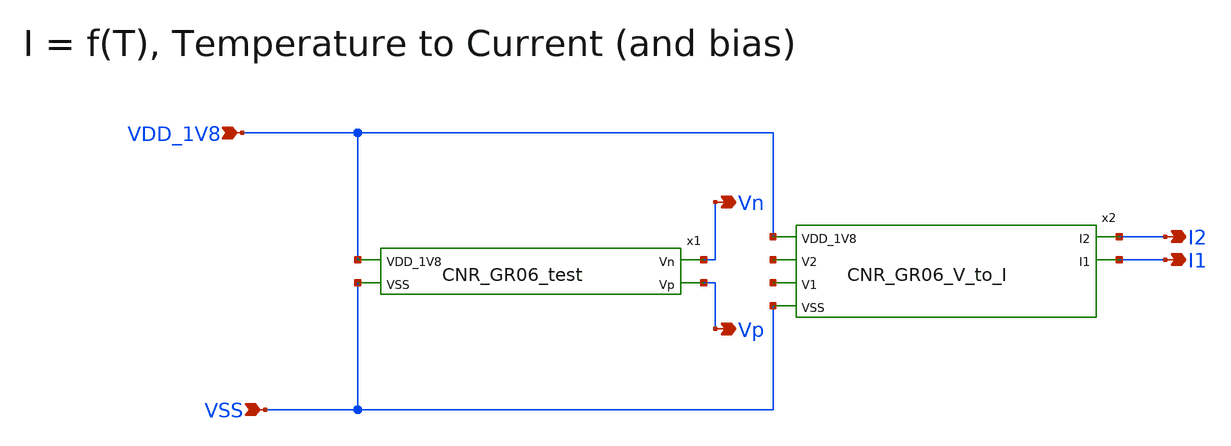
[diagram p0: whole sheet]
** sch_path: design/CNR_GR06_SKY130NM/CNR_GR06.sch
**.subckt CNR_GR06 VDD_1V8 VSS I2 I1 Vn Vp
*.ipin VDD_1V8
*.ipin VSS
*.opin I2
*.opin I1
*.opin Vn
*.opin Vp
x1 VDD_1V8 Vn Vp VSS CNR_GR06_test
x2 VDD_1V8 I2 I1 net1 net2 VSS CNR_GR06_V_to_I
**.ends

* expanding   symbol:  CNR_GR06_SKY130NM/CNR_GR06_test.sym # of pins=4
** sym_path: design/CNR_GR06_SKY130NM/CNR_GR06_test.sym
** sch_path: design/CNR_GR06_SKY130NM/CNR_GR06_test.sch
.subckt CNR_GR06_test VDD_1V8 Vn Vp VSS
*.ipin VSS
*.opin Vn
*.opin Vp
*.ipin VDD_1V8
XM1 net14 net1 VDD_1V8 VDD_1V8 sky130_fd_pr__pfet_01v8 L=1 W=20 nf=1 ad='int((nf+1)/2) * W/nf * 0.29'
+ as='int((nf+2)/2) * W/nf * 0.29' pd='2*int((nf+1)/2) * (W/nf + 0.29)' ps='2*int((nf+2)/2) * (W/nf + 0.29)'
+ nrd='0.29 / W' nrs='0.29 / W' sa=0 sb=0 sd=0 mult=1 m=1
XM3 net1 net1 VDD_1V8 VDD_1V8 sky130_fd_pr__pfet_01v8 L=1 W=20 nf=1 ad='int((nf+1)/2) * W/nf * 0.29'
+ as='int((nf+2)/2) * W/nf * 0.29' pd='2*int((nf+1)/2) * (W/nf + 0.29)' ps='2*int((nf+2)/2) * (W/nf + 0.29)'
+ nrd='0.29 / W' nrs='0.29 / W' sa=0 sb=0 sd=0 mult=1 m=1
XM4 net1 net1 VDD_1V8 VDD_1V8 sky130_fd_pr__pfet_01v8 L=1 W=20 nf=1 ad='int((nf+1)/2) * W/nf * 0.29'
+ as='int((nf+2)/2) * W/nf * 0.29' pd='2*int((nf+1)/2) * (W/nf + 0.29)' ps='2*int((nf+2)/2) * (W/nf + 0.29)'
+ nrd='0.29 / W' nrs='0.29 / W' sa=0 sb=0 sd=0 mult=1 m=1
XM5 net15 net1 VDD_1V8 VDD_1V8 sky130_fd_pr__pfet_01v8 L=1 W=20 nf=1 ad='int((nf+1)/2) * W/nf * 0.29'
+ as='int((nf+2)/2) * W/nf * 0.29' pd='2*int((nf+1)/2) * (W/nf + 0.29)' ps='2*int((nf+2)/2) * (W/nf + 0.29)'
+ nrd='0.29 / W' nrs='0.29 / W' sa=0 sb=0 sd=0 mult=1 m=1
XM6 net3 net2 net14 VDD_1V8 sky130_fd_pr__pfet_01v8 L=1 W=20 nf=1 ad='int((nf+1)/2) * W/nf * 0.29' as='int((nf+2)/2) * W/nf * 0.29'
+ pd='2*int((nf+1)/2) * (W/nf + 0.29)' ps='2*int((nf+2)/2) * (W/nf + 0.29)' nrd='0.29 / W' nrs='0.29 / W'
+ sa=0 sb=0 sd=0 mult=1 m=1
XM8 net2 net2 net1 VDD_1V8 sky130_fd_pr__pfet_01v8 L=1 W=20 nf=1 ad='int((nf+1)/2) * W/nf * 0.29' as='int((nf+2)/2) * W/nf * 0.29'
+ pd='2*int((nf+1)/2) * (W/nf + 0.29)' ps='2*int((nf+2)/2) * (W/nf + 0.29)' nrd='0.29 / W' nrs='0.29 / W'
+ sa=0 sb=0 sd=0 mult=1 m=1
XM9 net2 net2 net1 VDD_1V8 sky130_fd_pr__pfet_01v8 L=1 W=20 nf=1 ad='int((nf+1)/2) * W/nf * 0.29' as='int((nf+2)/2) * W/nf * 0.29'
+ pd='2*int((nf+1)/2) * (W/nf + 0.29)' ps='2*int((nf+2)/2) * (W/nf + 0.29)' nrd='0.29 / W' nrs='0.29 / W'
+ sa=0 sb=0 sd=0 mult=1 m=1
XM10 net4 net2 net15 VDD_1V8 sky130_fd_pr__pfet_01v8 L=1 W=20 nf=1 ad='int((nf+1)/2) * W/nf * 0.29' as='int((nf+2)/2) * W/nf * 0.29'
+ pd='2*int((nf+1)/2) * (W/nf + 0.29)' ps='2*int((nf+2)/2) * (W/nf + 0.29)' nrd='0.29 / W' nrs='0.29 / W'
+ sa=0 sb=0 sd=0 mult=1 m=1
XM11 net3 net3 VSS VSS sky130_fd_pr__nfet_01v8 L=1 W=10 nf=1 ad='int((nf+1)/2) * W/nf * 0.29' as='int((nf+2)/2) * W/nf * 0.29'
+ pd='2*int((nf+1)/2) * (W/nf + 0.29)' ps='2*int((nf+2)/2) * (W/nf + 0.29)' nrd='0.29 / W' nrs='0.29 / W'
+ sa=0 sb=0 sd=0 mult=1 m=1
XM12 net2 net3 net5 VSS sky130_fd_pr__nfet_01v8 L=1 W=10 nf=1 ad='int((nf+1)/2) * W/nf * 0.29' as='int((nf+2)/2) * W/nf * 0.29'
+ pd='2*int((nf+1)/2) * (W/nf + 0.29)' ps='2*int((nf+2)/2) * (W/nf + 0.29)' nrd='0.29 / W' nrs='0.29 / W'
+ sa=0 sb=0 sd=0 mult=1 m=1
XM13 net4 net4 net6 VSS sky130_fd_pr__nfet_01v8 L=1 W=10 nf=1 ad='int((nf+1)/2) * W/nf * 0.29' as='int((nf+2)/2) * W/nf * 0.29'
+ pd='2*int((nf+1)/2) * (W/nf + 0.29)' ps='2*int((nf+2)/2) * (W/nf + 0.29)' nrd='0.29 / W' nrs='0.29 / W'
+ sa=0 sb=0 sd=0 mult=1 m=1
XM14 net6 net4 net7 VSS sky130_fd_pr__nfet_01v8 L=1 W=10 nf=1 ad='int((nf+1)/2) * W/nf * 0.29' as='int((nf+2)/2) * W/nf * 0.29'
+ pd='2*int((nf+1)/2) * (W/nf + 0.29)' ps='2*int((nf+2)/2) * (W/nf + 0.29)' nrd='0.29 / W' nrs='0.29 / W'
+ sa=0 sb=0 sd=0 mult=1 m=1
XM15 net7 net4 VSS VSS sky130_fd_pr__nfet_01v8 L=1 W=10 nf=1 ad='int((nf+1)/2) * W/nf * 0.29' as='int((nf+2)/2) * W/nf * 0.29'
+ pd='2*int((nf+1)/2) * (W/nf + 0.29)' ps='2*int((nf+2)/2) * (W/nf + 0.29)' nrd='0.29 / W' nrs='0.29 / W'
+ sa=0 sb=0 sd=0 mult=1 m=1
XM16 net5 net2 VSS VSS sky130_fd_pr__nfet_01v8 L=1 W=10 nf=1 ad='int((nf+1)/2) * W/nf * 0.29' as='int((nf+2)/2) * W/nf * 0.29'
+ pd='2*int((nf+1)/2) * (W/nf + 0.29)' ps='2*int((nf+2)/2) * (W/nf + 0.29)' nrd='0.29 / W' nrs='0.29 / W'
+ sa=0 sb=0 sd=0 mult=1 m=1
XM17 net2 net2 net7 VSS sky130_fd_pr__nfet_01v8 L=1 W=10 nf=1 ad='int((nf+1)/2) * W/nf * 0.29' as='int((nf+2)/2) * W/nf * 0.29'
+ pd='2*int((nf+1)/2) * (W/nf + 0.29)' ps='2*int((nf+2)/2) * (W/nf + 0.29)' nrd='0.29 / W' nrs='0.29 / W'
+ sa=0 sb=0 sd=0 mult=1 m=1
XM18 net8 net2 VDD_1V8 VDD_1V8 sky130_fd_pr__pfet_01v8 L=1 W=20 nf=1 ad='int((nf+1)/2) * W/nf * 0.29'
+ as='int((nf+2)/2) * W/nf * 0.29' pd='2*int((nf+1)/2) * (W/nf + 0.29)' ps='2*int((nf+2)/2) * (W/nf + 0.29)'
+ nrd='0.29 / W' nrs='0.29 / W' sa=0 sb=0 sd=0 mult=1 m=1
XM19 Vn net2 VDD_1V8 VDD_1V8 sky130_fd_pr__pfet_01v8 L=1 W=20 nf=1 ad='int((nf+1)/2) * W/nf * 0.29' as='int((nf+2)/2) * W/nf * 0.29'
+ pd='2*int((nf+1)/2) * (W/nf + 0.29)' ps='2*int((nf+2)/2) * (W/nf + 0.29)' nrd='0.29 / W' nrs='0.29 / W'
+ sa=0 sb=0 sd=0 mult=1 m=1
XM20 net8 Vn net9 VSS sky130_fd_pr__nfet_01v8 L=1 W=10 nf=1 ad='int((nf+1)/2) * W/nf * 0.29' as='int((nf+2)/2) * W/nf * 0.29'
+ pd='2*int((nf+1)/2) * (W/nf + 0.29)' ps='2*int((nf+2)/2) * (W/nf + 0.29)' nrd='0.29 / W' nrs='0.29 / W'
+ sa=0 sb=0 sd=0 mult=1 m=1
XM21 net9 net9 net10 VSS sky130_fd_pr__nfet_01v8 L=1 W=10 nf=1 ad='int((nf+1)/2) * W/nf * 0.29' as='int((nf+2)/2) * W/nf * 0.29'
+ pd='2*int((nf+1)/2) * (W/nf + 0.29)' ps='2*int((nf+2)/2) * (W/nf + 0.29)' nrd='0.29 / W' nrs='0.29 / W'
+ sa=0 sb=0 sd=0 mult=1 m=1
XM22 Vn Vn net10 VSS sky130_fd_pr__nfet_01v8 L=1 W=10 nf=1 ad='int((nf+1)/2) * W/nf * 0.29' as='int((nf+2)/2) * W/nf * 0.29'
+ pd='2*int((nf+1)/2) * (W/nf + 0.29)' ps='2*int((nf+2)/2) * (W/nf + 0.29)' nrd='0.29 / W' nrs='0.29 / W'
+ sa=0 sb=0 sd=0 mult=1 m=1
XM23 net10 net9 VSS VSS sky130_fd_pr__nfet_01v8 L=1 W=10 nf=1 ad='int((nf+1)/2) * W/nf * 0.29' as='int((nf+2)/2) * W/nf * 0.29'
+ pd='2*int((nf+1)/2) * (W/nf + 0.29)' ps='2*int((nf+2)/2) * (W/nf + 0.29)' nrd='0.29 / W' nrs='0.29 / W'
+ sa=0 sb=0 sd=0 mult=1 m=1
XM24 net12 net12 net11 VDD_1V8 sky130_fd_pr__pfet_01v8 L=1 W=20 nf=1 ad='int((nf+1)/2) * W/nf * 0.29'
+ as='int((nf+2)/2) * W/nf * 0.29' pd='2*int((nf+1)/2) * (W/nf + 0.29)' ps='2*int((nf+2)/2) * (W/nf + 0.29)'
+ nrd='0.29 / W' nrs='0.29 / W' sa=0 sb=0 sd=0 mult=1 m=1
XM25 Vp Vp net11 VDD_1V8 sky130_fd_pr__pfet_01v8 L=1 W=20 nf=1 ad='int((nf+1)/2) * W/nf * 0.29' as='int((nf+2)/2) * W/nf * 0.29'
+ pd='2*int((nf+1)/2) * (W/nf + 0.29)' ps='2*int((nf+2)/2) * (W/nf + 0.29)' nrd='0.29 / W' nrs='0.29 / W'
+ sa=0 sb=0 sd=0 mult=1 m=1
XM26 net11 net12 VDD_1V8 VDD_1V8 sky130_fd_pr__pfet_01v8 L=1 W=20 nf=1 ad='int((nf+1)/2) * W/nf * 0.29'
+ as='int((nf+2)/2) * W/nf * 0.29' pd='2*int((nf+1)/2) * (W/nf + 0.29)' ps='2*int((nf+2)/2) * (W/nf + 0.29)'
+ nrd='0.29 / W' nrs='0.29 / W' sa=0 sb=0 sd=0 mult=1 m=1
XM27 net13 Vp net12 VDD_1V8 sky130_fd_pr__pfet_01v8 L=1 W=20 nf=1 ad='int((nf+1)/2) * W/nf * 0.29' as='int((nf+2)/2) * W/nf * 0.29'
+ pd='2*int((nf+1)/2) * (W/nf + 0.29)' ps='2*int((nf+2)/2) * (W/nf + 0.29)' nrd='0.29 / W' nrs='0.29 / W'
+ sa=0 sb=0 sd=0 mult=1 m=1
XM28 net13 net3 VSS VSS sky130_fd_pr__nfet_01v8 L=1 W=10 nf=1 ad='int((nf+1)/2) * W/nf * 0.29' as='int((nf+2)/2) * W/nf * 0.29'
+ pd='2*int((nf+1)/2) * (W/nf + 0.29)' ps='2*int((nf+2)/2) * (W/nf + 0.29)' nrd='0.29 / W' nrs='0.29 / W'
+ sa=0 sb=0 sd=0 mult=1 m=1
XM29 Vp net3 VSS VSS sky130_fd_pr__nfet_01v8 L=1 W=10 nf=1 ad='int((nf+1)/2) * W/nf * 0.29' as='int((nf+2)/2) * W/nf * 0.29'
+ pd='2*int((nf+1)/2) * (W/nf + 0.29)' ps='2*int((nf+2)/2) * (W/nf + 0.29)' nrd='0.29 / W' nrs='0.29 / W'
+ sa=0 sb=0 sd=0 mult=1 m=1
.ends


* expanding   symbol:  CNR_GR06_SKY130NM/CNR_GR06_V_to_I.sym # of pins=6
** sym_path: design/CNR_GR06_SKY130NM/CNR_GR06_V_to_I.sym
** sch_path: design/CNR_GR06_SKY130NM/CNR_GR06_V_to_I.sch
.subckt CNR_GR06_V_to_I VDD_1V8 I2 I1 V2 V1 VSS
*.ipin VDD_1V8
*.ipin VSS
*.opin I1
*.opin I2
*.ipin V1
*.ipin V2
XM6 VDD_1V8 net1 net1 GND sky130_fd_pr__nfet_01v8 L=0.15 W=1 nf=1 ad='int((nf+1)/2) * W/nf * 0.29' as='int((nf+2)/2) * W/nf * 0.29'
+ pd='2*int((nf+1)/2) * (W/nf + 0.29)' ps='2*int((nf+2)/2) * (W/nf + 0.29)' nrd='0.29 / W' nrs='0.29 / W'
+ sa=0 sb=0 sd=0 mult=1 m=1
XM1 VDD_1V8 net1 I1 GND sky130_fd_pr__nfet_01v8 L=0.15 W=1 nf=1 ad='int((nf+1)/2) * W/nf * 0.29' as='int((nf+2)/2) * W/nf * 0.29'
+ pd='2*int((nf+1)/2) * (W/nf + 0.29)' ps='2*int((nf+2)/2) * (W/nf + 0.29)' nrd='0.29 / W' nrs='0.29 / W'
+ sa=0 sb=0 sd=0 mult=1 m=1
XM2 VDD_1V8 net2 net2 GND sky130_fd_pr__nfet_01v8 L=0.15 W=1 nf=1 ad='int((nf+1)/2) * W/nf * 0.29' as='int((nf+2)/2) * W/nf * 0.29'
+ pd='2*int((nf+1)/2) * (W/nf + 0.29)' ps='2*int((nf+2)/2) * (W/nf + 0.29)' nrd='0.29 / W' nrs='0.29 / W'
+ sa=0 sb=0 sd=0 mult=1 m=1
XM3 VDD_1V8 net2 I2 GND sky130_fd_pr__nfet_01v8 L=0.15 W=1 nf=1 ad='int((nf+1)/2) * W/nf * 0.29' as='int((nf+2)/2) * W/nf * 0.29'
+ pd='2*int((nf+1)/2) * (W/nf + 0.29)' ps='2*int((nf+2)/2) * (W/nf + 0.29)' nrd='0.29 / W' nrs='0.29 / W'
+ sa=0 sb=0 sd=0 mult=1 m=1
XM4 net2 V2 VSS GND sky130_fd_pr__nfet_01v8 L=0.15 W=1 nf=1 ad='int((nf+1)/2) * W/nf * 0.29' as='int((nf+2)/2) * W/nf * 0.29'
+ pd='2*int((nf+1)/2) * (W/nf + 0.29)' ps='2*int((nf+2)/2) * (W/nf + 0.29)' nrd='0.29 / W' nrs='0.29 / W'
+ sa=0 sb=0 sd=0 mult=1 m=1
XM5 net1 V1 VSS GND sky130_fd_pr__nfet_01v8 L=0.15 W=1 nf=1 ad='int((nf+1)/2) * W/nf * 0.29' as='int((nf+2)/2) * W/nf * 0.29'
+ pd='2*int((nf+1)/2) * (W/nf + 0.29)' ps='2*int((nf+2)/2) * (W/nf + 0.29)' nrd='0.29 / W' nrs='0.29 / W'
+ sa=0 sb=0 sd=0 mult=1 m=1
.ends

.end
